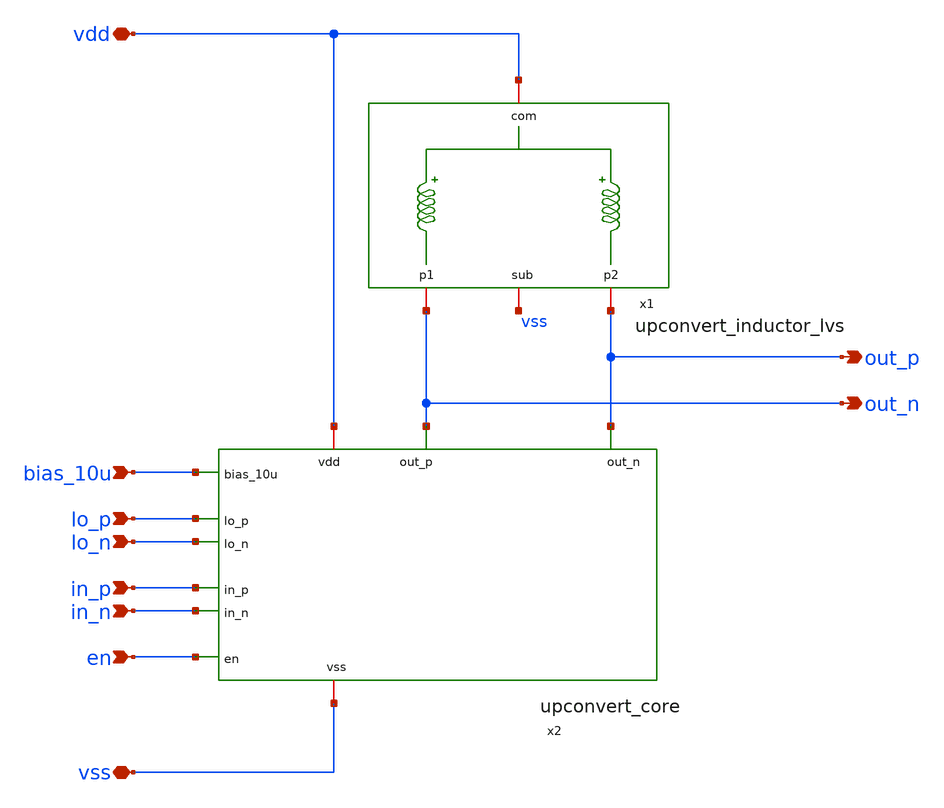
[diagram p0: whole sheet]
** sch_path: design/upconvert/upconvert.sch
**.subckt upconvert in_n in_p bias_10u vss vdd out_p out_n en lo_n lo_p
*.ipin in_n
*.ipin in_p
*.ipin bias_10u
*.iopin vss
*.iopin vdd
*.opin out_p
*.opin out_n
*.ipin en
*.ipin lo_n
*.ipin lo_p
x1 vdd out_p out_n vss upconvert_inductor_lvs
x2 vdd en in_p in_n out_n out_p lo_p lo_n bias_10u vss upconvert_core
**.ends
.end
